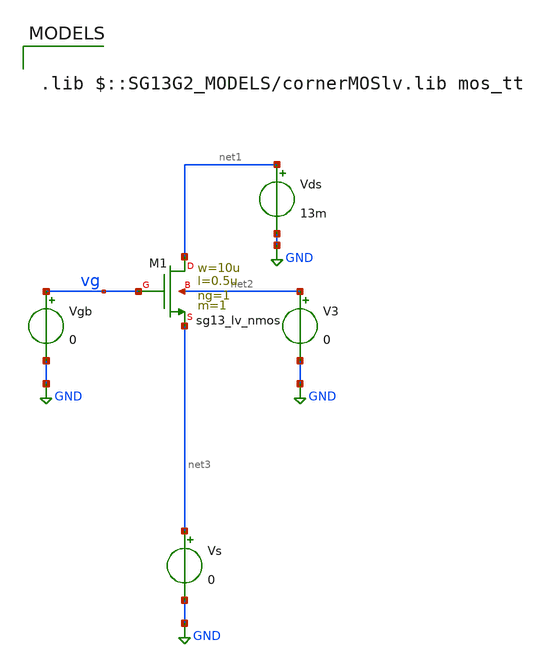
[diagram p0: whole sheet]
** sch_path: ihp_tutorials/Extraction/nmos_ext.sch
**.subckt nmos_ext
Vds net1 GND 13m
V3 net2 GND 0
Vs net3 GND 0
Vgb vg GND 0
XM1 net1 vg net3 net2 sg13_lv_nmos w=10u l=0.5u ng=1 m=1 mm_ok=1
**** begin user architecture code

.lib $::SG13G2_MODELS/cornerMOSlv.lib mos_tt



.option gmin = 1e-24

.control
pre_osdi ./psp103_nqs.osdi
save all
dc Vgb -0.1 1.5 1m

let gm_id = deriv(ln(i(Vs)))
save gm_id

meas dc gm_id_max MAX gm_id
let gm_id_vt = 0.531*gm_id_max
save gm_id_vt

meas dc vt0 FIND V(vg) WHEN gm_id=gm_id_vt
meas dc is_ FIND i(Vs) WHEN V(vg)=vt0

let is = is_/0.88
let VT_val=0.026
let n = 1/(gm_id_max*VT_val)
save is vt0 n
echo
echo
echo

echo Extracted parameters:
print is vt0 n


echo
echo
echo

remzerovec
write nmos_ext.raw

.endc



**** end user architecture code
**.ends
.GLOBAL GND
.end
